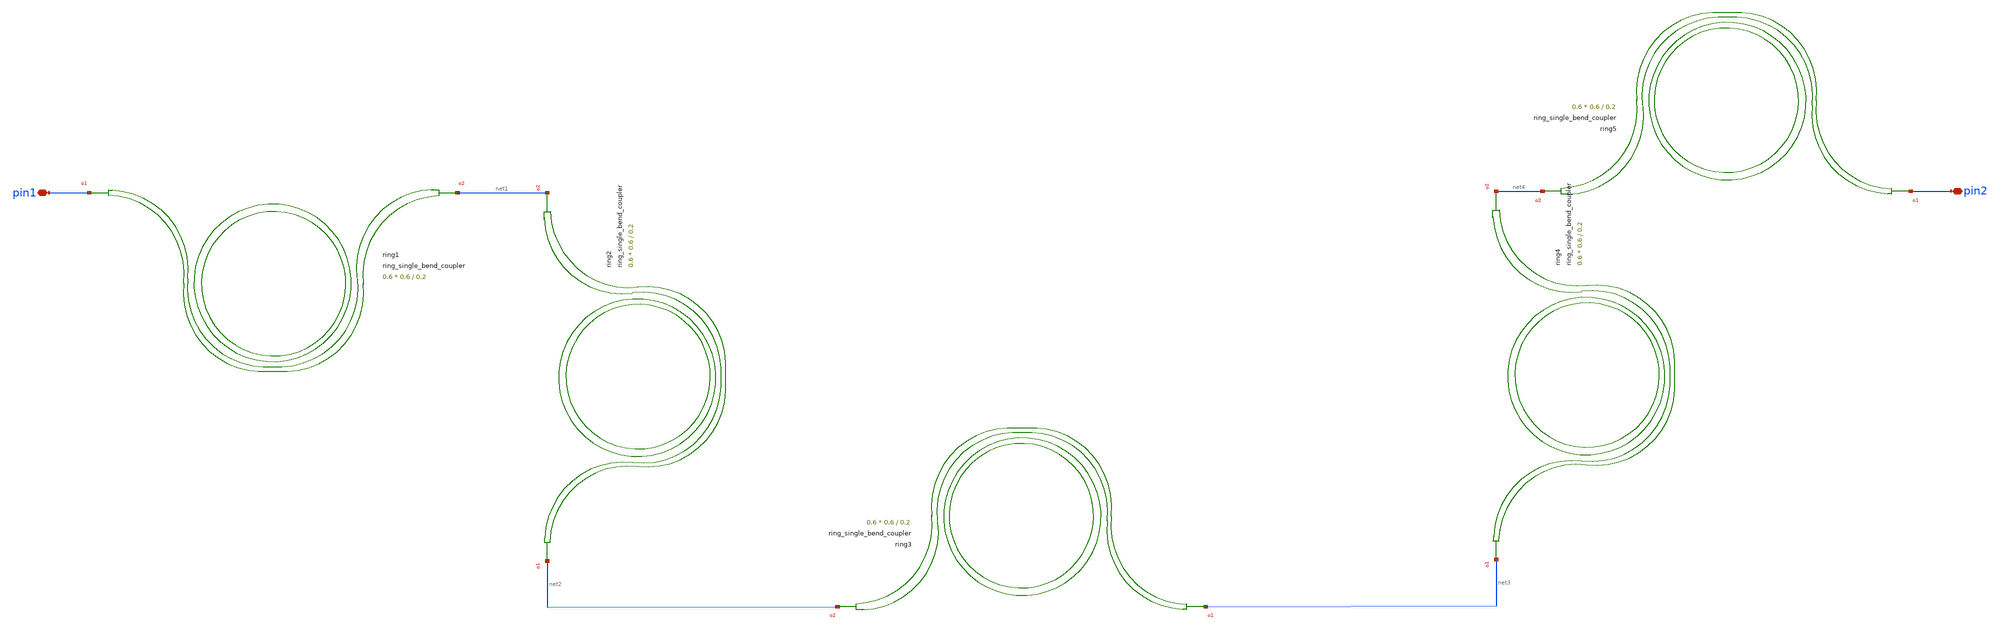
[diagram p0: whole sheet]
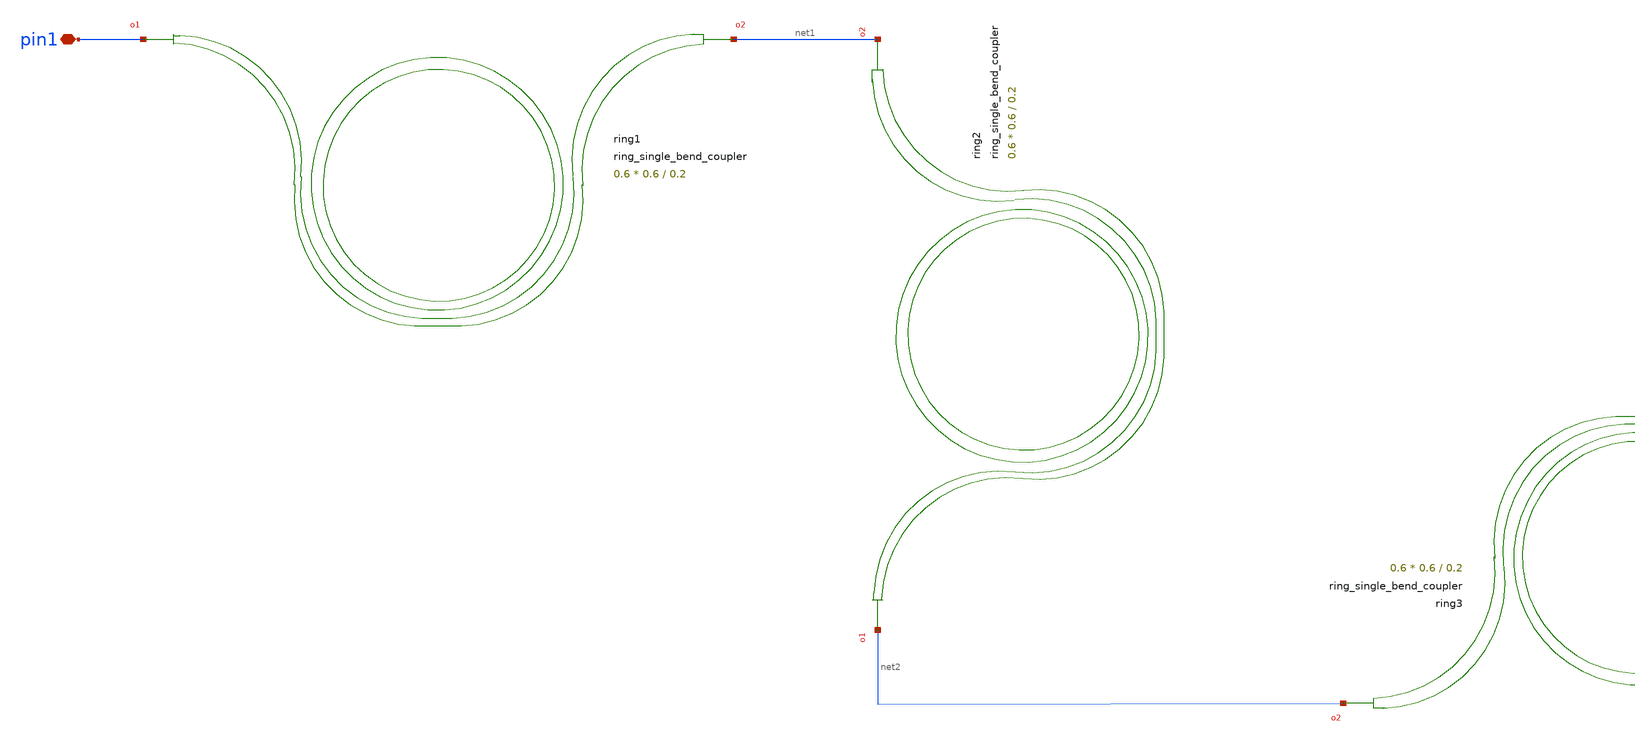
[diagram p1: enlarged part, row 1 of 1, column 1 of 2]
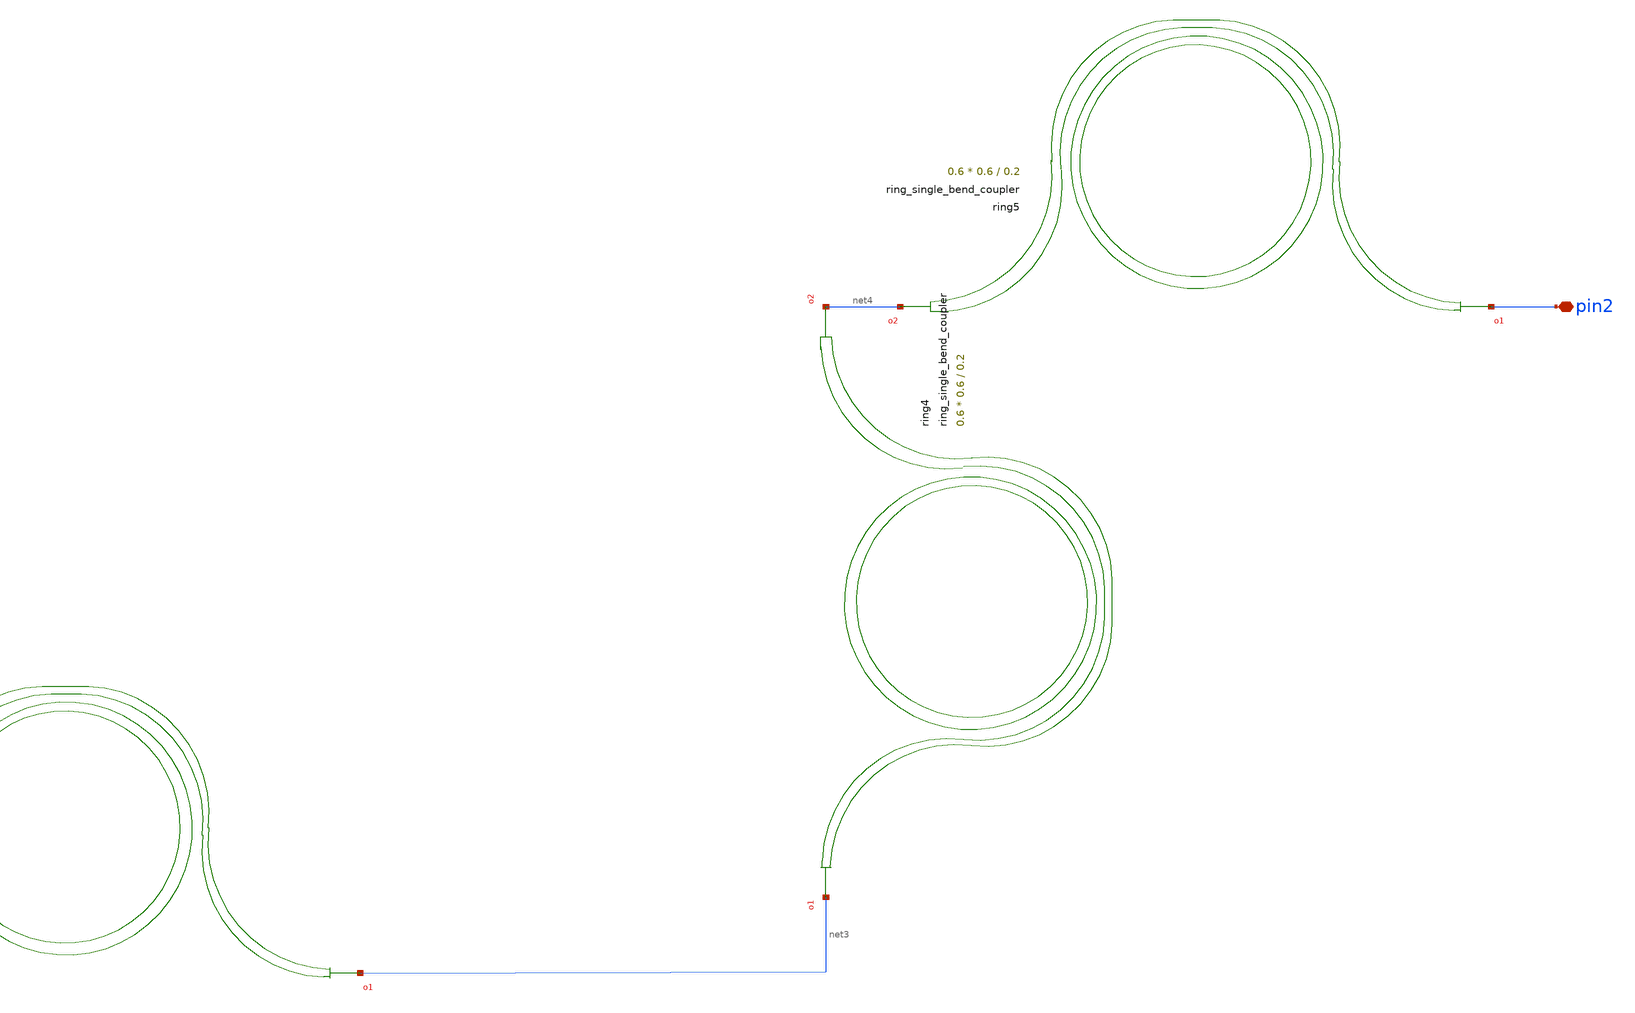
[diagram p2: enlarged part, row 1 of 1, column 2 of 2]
** sch_path: cells/xschem/tests/test_ring_single_bend_coupler.sch
* SPDX-FileCopyrightText: 2023 Mabrains Company
* Licensed under the GNU GENERAL PUBLIC License, Version 3.0 (the "License");
* you may not use this file except in compliance with the License.
* GNU GENERAL PUBLIC LICENSE
* Version 3, 29 June 2007
* This program is free software: you can redistribute it and/or modify
* it under the terms of the GNU General Public License as published
* by the Free Software Foundation, either 3 of the License, or
* (at your option) any later version.
* This program is distributed in the hope that it will be useful,
* but WITHOUT ANY WARRANTY; without even the implied warranty of
* MERCHANTABILITY or FITNESS FOR A PARTICULAR PURPOSE.  See the
* GNU General Public License for more details.
* You should have received a copy of the GNU General Public License
* along with this program.  If not, see <https://www.gnu.org/licenses/>.
* SPDX-License-Identifier: GPL-3.0
**.subckt test_ring_single_bend_coupler pin1 pin2
*.iopin pin1
*.iopin pin2
Pring1 pin1 net1 ring_single_bend_coupler gap=0.2 radius=5.0 angle_inner=90 angle_outer=90
+ length_x=0.6 length_y=0.6
Pring2 net2 net1 ring_single_bend_coupler gap=0.2 radius=5.0 angle_inner=90 angle_outer=90
+ length_x=0.6 length_y=0.6
Pring3 net3 net2 ring_single_bend_coupler gap=0.2 radius=5.0 angle_inner=90 angle_outer=90
+ length_x=0.6 length_y=0.6
Pring4 net3 net4 ring_single_bend_coupler gap=0.2 radius=5.0 angle_inner=90 angle_outer=90
+ length_x=0.6 length_y=0.6
Pring5 pin2 net4 ring_single_bend_coupler gap=0.2 radius=5.0 angle_inner=90 angle_outer=90
+ length_x=0.6 length_y=0.6
**.ends
.end
